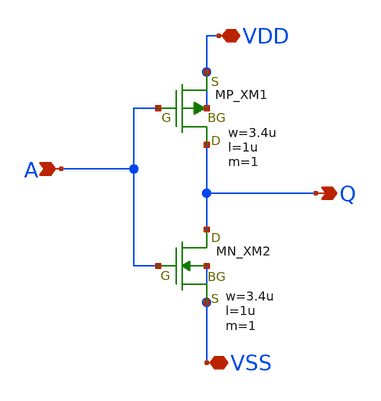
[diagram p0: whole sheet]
** sch_path: member_project/inverter/ShinriNakamura/inverter.sch
**.subckt inverter VDD VSS A Q
*.iopin VDD
*.iopin VSS
*.ipin A
*.opin Q
XM1 Q A VDD VDD PMOS w=3.4u l=1u as=0 ad=0 ps=0 pd=0 nrd=0 nrs=0 m=1
XM2 Q A VSS VSS NMOS w=3.4u l=1u as=0 ad=0 ps=0 pd=0 nrd=0 nrs=0 m=1
**.ends
.end
